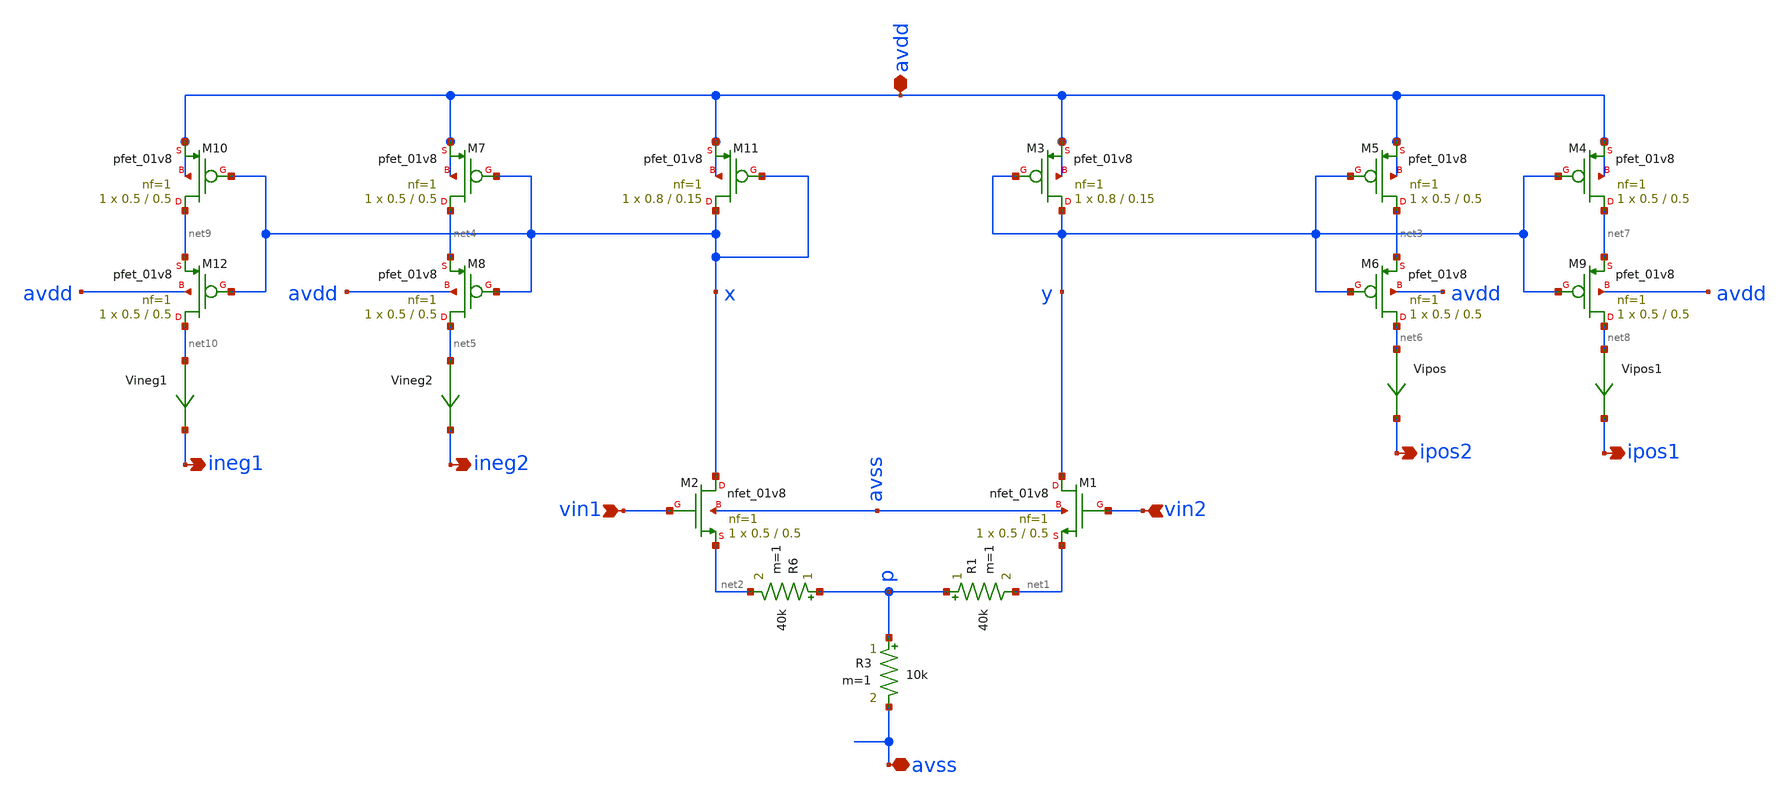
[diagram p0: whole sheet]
** sch_path: VCCS/otavccs4.sch
**.subckt otavccs4 avdd avss vin1 vin2 ineg2 ipos2 ipos1 ineg1
*.iopin avdd
*.iopin avss
*.ipin vin1
*.ipin vin2
*.opin ineg2
*.opin ipos2
*.opin ipos1
*.opin ineg1
XM2 x vin1 net2 avss sky130_fd_pr__nfet_01v8 L=0.5 W=0.5 nf=1 ad='int((1 + 1)/2) * 0.5 / 1 * 0.29' as='int((1 + 2)/2) * 0.5 / 1 * 0.29'
+ pd='2*int((1 + 1)/2) * (0.5 / 1 + 0.29)' ps='2*int((1 + 2)/2) * (0.5 / 1 + 0.29)' nrd='0.29 / 0.5 ' nrs='0.29 / 0.5 '
+ sa=0 sb=0 sd=0 mult=1 m=1
XM1 y vin2 net1 avss sky130_fd_pr__nfet_01v8 L=0.5 W=0.5 nf=1 ad='int((1 + 1)/2) * 0.5 / 1 * 0.29' as='int((1 + 2)/2) * 0.5 / 1 * 0.29'
+ pd='2*int((1 + 1)/2) * (0.5 / 1 + 0.29)' ps='2*int((1 + 2)/2) * (0.5 / 1 + 0.29)' nrd='0.29 / 0.5 ' nrs='0.29 / 0.5 '
+ sa=0 sb=0 sd=0 mult=1 m=1
XM11 x x avdd avdd sky130_fd_pr__pfet_01v8 L=0.15 W=0.8 nf=1 ad='int((nf+1)/2) * W/nf * 0.29' as='int((nf+2)/2) * W/nf * 0.29'
+ pd='2*int((nf+1)/2) * (W/nf + 0.29)' ps='2*int((nf+2)/2) * (W/nf + 0.29)' nrd='0.29 / W' nrs='0.29 / W'
+ sa=0 sb=0 sd=0 mult=1 m=1
XM3 y y avdd avdd sky130_fd_pr__pfet_01v8 L=0.15 W=0.8 nf=1 ad='int((nf+1)/2) * W/nf * 0.29' as='int((nf+2)/2) * W/nf * 0.29'
+ pd='2*int((nf+1)/2) * (W/nf + 0.29)' ps='2*int((nf+2)/2) * (W/nf + 0.29)' nrd='0.29 / W' nrs='0.29 / W'
+ sa=0 sb=0 sd=0 mult=1 m=1
XM5 net3 y avdd avdd sky130_fd_pr__pfet_01v8 L=0.5 W=0.5 nf=1 ad='int((nf+1)/2) * W/nf * 0.29' as='int((nf+2)/2) * W/nf * 0.29'
+ pd='2*int((nf+1)/2) * (W/nf + 0.29)' ps='2*int((nf+2)/2) * (W/nf + 0.29)' nrd='0.29 / W' nrs='0.29 / W'
+ sa=0 sb=0 sd=0 mult=1 m=1
XM6 net6 y net3 avdd sky130_fd_pr__pfet_01v8 L=0.5 W=0.5 nf=1 ad='int((nf+1)/2) * W/nf * 0.29' as='int((nf+2)/2) * W/nf * 0.29'
+ pd='2*int((nf+1)/2) * (W/nf + 0.29)' ps='2*int((nf+2)/2) * (W/nf + 0.29)' nrd='0.29 / W' nrs='0.29 / W'
+ sa=0 sb=0 sd=0 mult=1 m=1
Vipos net6 ipos2 0
.save i(vipos)
XM7 net4 x avdd avdd sky130_fd_pr__pfet_01v8 L=0.5 W=0.5 nf=1 ad='int((nf+1)/2) * W/nf * 0.29' as='int((nf+2)/2) * W/nf * 0.29'
+ pd='2*int((nf+1)/2) * (W/nf + 0.29)' ps='2*int((nf+2)/2) * (W/nf + 0.29)' nrd='0.29 / W' nrs='0.29 / W'
+ sa=0 sb=0 sd=0 mult=1 m=1
XM8 net5 x net4 avdd sky130_fd_pr__pfet_01v8 L=0.5 W=0.5 nf=1 ad='int((nf+1)/2) * W/nf * 0.29' as='int((nf+2)/2) * W/nf * 0.29'
+ pd='2*int((nf+1)/2) * (W/nf + 0.29)' ps='2*int((nf+2)/2) * (W/nf + 0.29)' nrd='0.29 / W' nrs='0.29 / W'
+ sa=0 sb=0 sd=0 mult=1 m=1
Vineg2 net5 ineg2 0
.save i(vineg2)
R3 p avss 10k m=1
R6 p net2 40k m=1
R1 p net1 40k m=1
XM4 net7 y avdd avdd sky130_fd_pr__pfet_01v8 L=0.5 W=0.5 nf=1 ad='int((nf+1)/2) * W/nf * 0.29' as='int((nf+2)/2) * W/nf * 0.29'
+ pd='2*int((nf+1)/2) * (W/nf + 0.29)' ps='2*int((nf+2)/2) * (W/nf + 0.29)' nrd='0.29 / W' nrs='0.29 / W'
+ sa=0 sb=0 sd=0 mult=1 m=1
XM9 net8 y net7 avdd sky130_fd_pr__pfet_01v8 L=0.5 W=0.5 nf=1 ad='int((nf+1)/2) * W/nf * 0.29' as='int((nf+2)/2) * W/nf * 0.29'
+ pd='2*int((nf+1)/2) * (W/nf + 0.29)' ps='2*int((nf+2)/2) * (W/nf + 0.29)' nrd='0.29 / W' nrs='0.29 / W'
+ sa=0 sb=0 sd=0 mult=1 m=1
Vipos1 net8 ipos1 0
.save i(vipos1)
XM10 net9 x avdd avdd sky130_fd_pr__pfet_01v8 L=0.5 W=0.5 nf=1 ad='int((nf+1)/2) * W/nf * 0.29' as='int((nf+2)/2) * W/nf * 0.29'
+ pd='2*int((nf+1)/2) * (W/nf + 0.29)' ps='2*int((nf+2)/2) * (W/nf + 0.29)' nrd='0.29 / W' nrs='0.29 / W'
+ sa=0 sb=0 sd=0 mult=1 m=1
XM12 net10 x net9 avdd sky130_fd_pr__pfet_01v8 L=0.5 W=0.5 nf=1 ad='int((nf+1)/2) * W/nf * 0.29' as='int((nf+2)/2) * W/nf * 0.29'
+ pd='2*int((nf+1)/2) * (W/nf + 0.29)' ps='2*int((nf+2)/2) * (W/nf + 0.29)' nrd='0.29 / W' nrs='0.29 / W'
+ sa=0 sb=0 sd=0 mult=1 m=1
Vineg1 net10 ineg1 0
.save i(vineg1)
**.ends
.end
